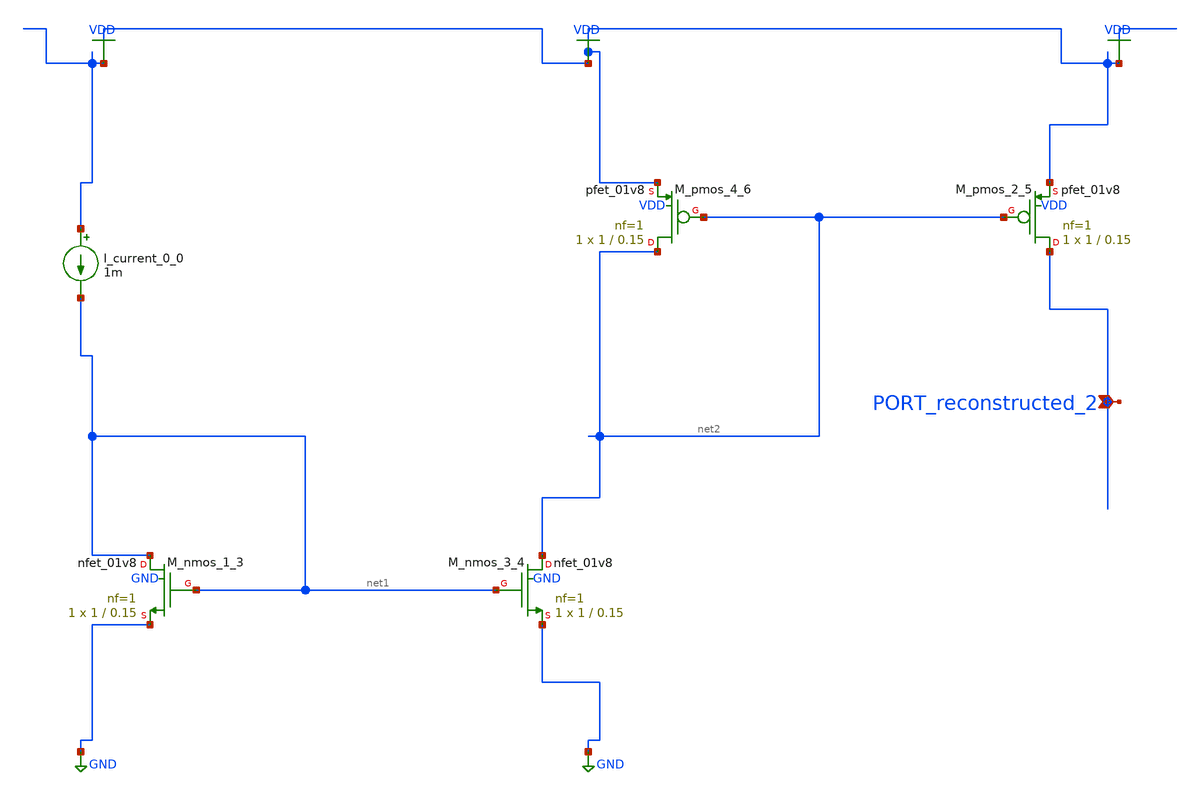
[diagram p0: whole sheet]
** sch_path: schematics/AMSNet/254.sch
**.subckt 254 PORT_reconstructed_2
*.ipin PORT_reconstructed_2
I_current_0_0 VDD net1 1m
XM_nmos_1_3 net1 net1 GND GND sky130_fd_pr__nfet_01v8 L=0.15 W=1 nf=1 ad='int((1 + 1)/2) * 1 / 1 * 0.29'
+ as='int((1 + 2)/2) * 1 / 1 * 0.29' pd='2*int((1 + 1)/2) * (1 / 1 + 0.29)' ps='2*int((1 + 2)/2) * (1 / 1 + 0.29)'
+ nrd='0.29 / 1 ' nrs='0.29 / 1 ' sa=0 sb=0 sd=0 mult=1 m=1
XM_nmos_3_4 net2 net1 GND GND sky130_fd_pr__nfet_01v8 L=0.15 W=1 nf=1 ad='int((1 + 1)/2) * 1 / 1 * 0.29'
+ as='int((1 + 2)/2) * 1 / 1 * 0.29' pd='2*int((1 + 1)/2) * (1 / 1 + 0.29)' ps='2*int((1 + 2)/2) * (1 / 1 + 0.29)'
+ nrd='0.29 / 1 ' nrs='0.29 / 1 ' sa=0 sb=0 sd=0 mult=1 m=1
XM_pmos_2_5 PORT_reconstructed_2 net2 VDD VDD sky130_fd_pr__pfet_01v8 L=0.15 W=1 nf=1 ad='int((1 + 1)/2) * 1 / 1 * 0.29'
+ as='int((1 + 2)/2) * 1 / 1 * 0.29' pd='2*int((1 + 1)/2) * (1 / 1 + 0.29)' ps='2*int((1 + 2)/2) * (1 / 1 + 0.29)'
+ nrd='0.29 / 1 ' nrs='0.29 / 1 ' sa=0 sb=0 sd=0 mult=1 m=1
XM_pmos_4_6 net2 net2 VDD VDD sky130_fd_pr__pfet_01v8 L=0.15 W=1 nf=1 ad='int((1 + 1)/2) * 1 / 1 * 0.29'
+ as='int((1 + 2)/2) * 1 / 1 * 0.29' pd='2*int((1 + 1)/2) * (1 / 1 + 0.29)' ps='2*int((1 + 2)/2) * (1 / 1 + 0.29)'
+ nrd='0.29 / 1 ' nrs='0.29 / 1 ' sa=0 sb=0 sd=0 mult=1 m=1
**.ends
.GLOBAL GND
.GLOBAL VDD
.end
